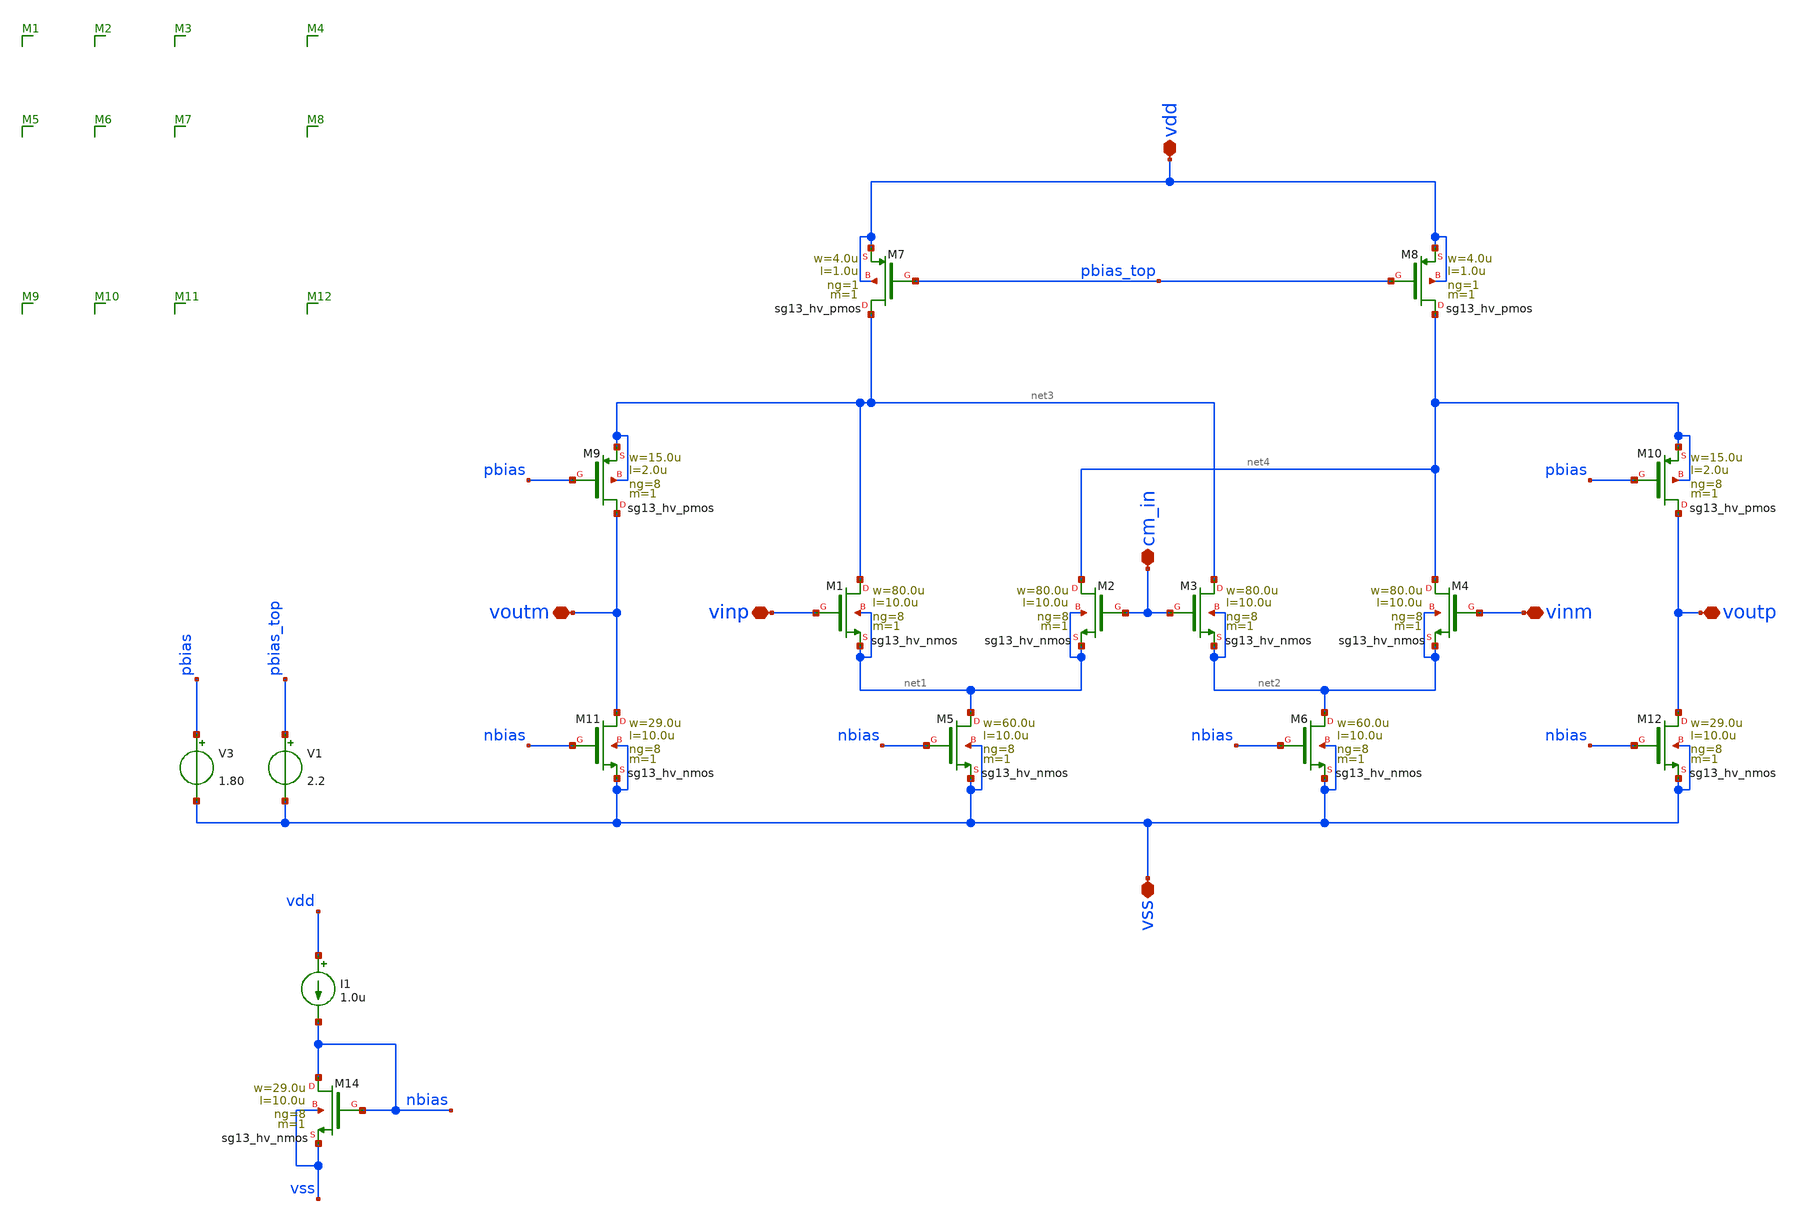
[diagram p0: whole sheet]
** sch_path: schematic/aux_amp.sch
**.subckt aux_amp vss voutm vinp vdd voutp vinm vinp cm_in
*.iopin vss
*.iopin voutm
*.iopin vinp
*.iopin vdd
*.iopin voutp
*.iopin vinm
*.iopin vinp
*.iopin cm_in
XM1 net3 vinp net1 net1 sg13_hv_nmos w=80.0u l=10.0u ng=8 m=1 mm_ok=1
XM2 net4 cm_in net1 net1 sg13_hv_nmos w=80.0u l=10.0u ng=8 m=1 mm_ok=1
XM5 net1 nbias vss vss sg13_hv_nmos w=60.0u l=10.0u ng=8 m=1 mm_ok=1
XM3 net3 cm_in net2 net2 sg13_hv_nmos w=80.0u l=10.0u ng=8 m=1 mm_ok=1
XM4 net4 vinm net2 net2 sg13_hv_nmos w=80.0u l=10.0u ng=8 m=1 mm_ok=1
XM6 net2 nbias vss vss sg13_hv_nmos w=60.0u l=10.0u ng=8 m=1 mm_ok=1
XM11 voutm nbias vss vss sg13_hv_nmos w=29.0u l=10.0u ng=8 m=1 mm_ok=1
XM12 voutp nbias vss vss sg13_hv_nmos w=29.0u l=10.0u ng=8 m=1 mm_ok=1
V3 pbias vss 1.80
XM9 voutm pbias net3 net3 sg13_hv_pmos w=15.0u l=2.0u ng=8 m=1 mm_ok=1
XM7 net3 pbias_top vdd vdd sg13_hv_pmos w=4.0u l=1.0u ng=1 m=1 mm_ok=1
XM8 net4 pbias_top vdd vdd sg13_hv_pmos w=4.0u l=1.0u ng=1 m=1 mm_ok=1
XM10 voutp pbias net4 net4 sg13_hv_pmos w=15.0u l=2.0u ng=8 m=1 mm_ok=1
XM14 nbias nbias vss vss sg13_hv_nmos w=29.0u l=10.0u ng=8 m=1 mm_ok=1
I1 vdd nbias 1.0u
V1 pbias_top vss 2.2
**.ends
.end
